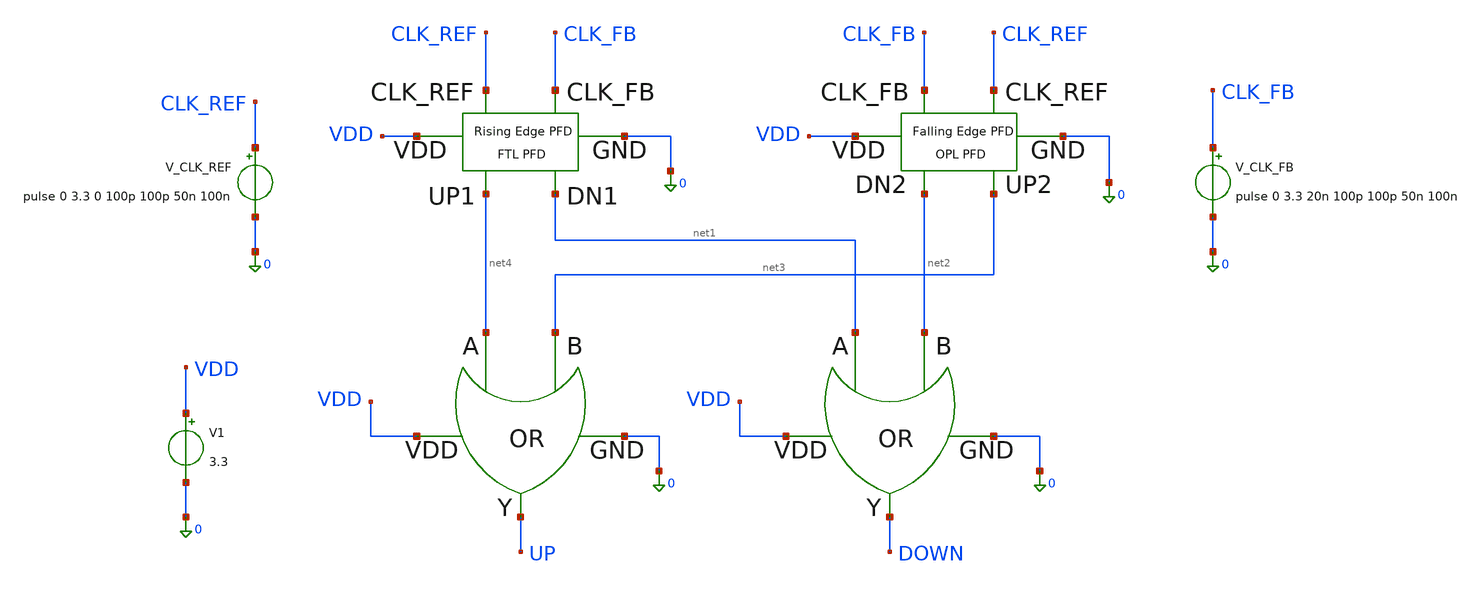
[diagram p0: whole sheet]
** sch_path: PFD/DELD_PFD.sch
**.subckt DELD_PFD
x1 0 net1 net2 VDD DOWN OR
x2 0 net4 net3 VDD UP OR
x3 net1 net4 CLK_FB CLK_REF VDD 0 FTL_PFD
x4 net3 net2 CLK_REF CLK_FB VDD 0 OPL_PFD
V1 VDD 0 3.3
.save i(v1)
V_CLK_REF CLK_REF 0 pulse 0 3.3 0 100p 100p 50n 100n
.save i(v_clk_ref)
V_CLK_FB CLK_FB 0 pulse 0 3.3 20n 100p 100p 50n 100n
.save i(v_clk_fb)
**.ends

* expanding   symbol:  OR.sym # of pins=5
** sym_path: PFD/OR.sym
** sch_path: PFD/OR.sch
.subckt OR GND A B VDD Y
*.opin Y
*.ipin GND
*.ipin VDD
*.ipin A
*.ipin B
XM3 net2 A GND GND nfet_03v3 L=0.28u W=0.22u nf=1 ad='int((nf+1)/2) * W/nf * 0.18u' as='int((nf+2)/2) * W/nf * 0.18u'
+ pd='2*int((nf+1)/2) * (W/nf + 0.18u)' ps='2*int((nf+2)/2) * (W/nf + 0.18u)' nrd='0.18u / W' nrs='0.18u / W'
+ sa=0 sb=0 sd=0 m=1
XM2 net1 A VDD VDD pfet_03v3 L=0.28u W=0.22u nf=1 ad='int((nf+1)/2) * W/nf * 0.18u' as='int((nf+2)/2) * W/nf * 0.18u'
+ pd='2*int((nf+1)/2) * (W/nf + 0.18u)' ps='2*int((nf+2)/2) * (W/nf + 0.18u)' nrd='0.18u / W' nrs='0.18u / W'
+ sa=0 sb=0 sd=0 m=3
XM4 net2 B net1 VDD pfet_03v3 L=0.28u W=0.22u nf=1 ad='int((nf+1)/2) * W/nf * 0.18u' as='int((nf+2)/2) * W/nf * 0.18u'
+ pd='2*int((nf+1)/2) * (W/nf + 0.18u)' ps='2*int((nf+2)/2) * (W/nf + 0.18u)' nrd='0.18u / W' nrs='0.18u / W'
+ sa=0 sb=0 sd=0 m=3
XM1 net2 B GND GND nfet_03v3 L=0.28u W=0.22u nf=1 ad='int((nf+1)/2) * W/nf * 0.18u' as='int((nf+2)/2) * W/nf * 0.18u'
+ pd='2*int((nf+1)/2) * (W/nf + 0.18u)' ps='2*int((nf+2)/2) * (W/nf + 0.18u)' nrd='0.18u / W' nrs='0.18u / W'
+ sa=0 sb=0 sd=0 m=1
XM29 Y net2 VDD VDD pfet_03v3 L=0.28u W=0.22u nf=1 ad='int((nf+1)/2) * W/nf * 0.18u' as='int((nf+2)/2) * W/nf * 0.18u'
+ pd='2*int((nf+1)/2) * (W/nf + 0.18u)' ps='2*int((nf+2)/2) * (W/nf + 0.18u)' nrd='0.18u / W' nrs='0.18u / W'
+ sa=0 sb=0 sd=0 m=3
XM30 Y net2 GND GND nfet_03v3 L=0.28u W=0.22u nf=1 ad='int((nf+1)/2) * W/nf * 0.18u' as='int((nf+2)/2) * W/nf * 0.18u'
+ pd='2*int((nf+1)/2) * (W/nf + 0.18u)' ps='2*int((nf+2)/2) * (W/nf + 0.18u)' nrd='0.18u / W' nrs='0.18u / W'
+ sa=0 sb=0 sd=0 m=1
.ends


* expanding   symbol:  FTL_PFD.sym # of pins=6
** sym_path: PFD/FTL_PFD.sym
** sch_path: PFD/FTL_PFD.sch
.subckt FTL_PFD DN1 UP1 CLK_FB CLK_REF VDD GND
*.opin UP1
*.opin DN1
*.ipin CLK_FB
*.ipin CLK_REF
*.iopin VDD
*.iopin GND
XM1 net1 net3 VDD VDD pfet_03v3 L=0.28u W=0.22u nf=1 ad='int((nf+1)/2) * W/nf * 0.18u' as='int((nf+2)/2) * W/nf * 0.18u'
+ pd='2*int((nf+1)/2) * (W/nf + 0.18u)' ps='2*int((nf+2)/2) * (W/nf + 0.18u)' nrd='0.18u / W' nrs='0.18u / W'
+ sa=0 sb=0 sd=0 m=1
XM4 net2 net3 GND GND nfet_03v3 L=0.28u W=0.22u nf=1 ad='int((nf+1)/2) * W/nf * 0.18u' as='int((nf+2)/2) * W/nf * 0.18u'
+ pd='2*int((nf+1)/2) * (W/nf + 0.18u)' ps='2*int((nf+2)/2) * (W/nf + 0.18u)' nrd='0.18u / W' nrs='0.18u / W'
+ sa=0 sb=0 sd=0 m=1
XM2 net2 CLK_REF net1 VDD pfet_03v3 L=0.28u W=0.22u nf=1 ad='int((nf+1)/2) * W/nf * 0.18u' as='int((nf+2)/2) * W/nf * 0.18u'
+ pd='2*int((nf+1)/2) * (W/nf + 0.18u)' ps='2*int((nf+2)/2) * (W/nf + 0.18u)' nrd='0.18u / W' nrs='0.18u / W'
+ sa=0 sb=0 sd=0 m=1
XM3 net2 CLK_REF GND GND nfet_03v3 L=0.28u W=0.22u nf=1 ad='int((nf+1)/2) * W/nf * 0.18u' as='int((nf+2)/2) * W/nf * 0.18u'
+ pd='2*int((nf+1)/2) * (W/nf + 0.18u)' ps='2*int((nf+2)/2) * (W/nf + 0.18u)' nrd='0.18u / W' nrs='0.18u / W'
+ sa=0 sb=0 sd=0 m=1
XM5 net4 net2 VDD VDD pfet_03v3 L=0.28u W=0.22u nf=1 ad='int((nf+1)/2) * W/nf * 0.18u' as='int((nf+2)/2) * W/nf * 0.18u'
+ pd='2*int((nf+1)/2) * (W/nf + 0.18u)' ps='2*int((nf+2)/2) * (W/nf + 0.18u)' nrd='0.18u / W' nrs='0.18u / W'
+ sa=0 sb=0 sd=0 m=1
XM6 net5 CLK_REF net4 VDD pfet_03v3 L=0.28u W=0.22u nf=1 ad='int((nf+1)/2) * W/nf * 0.18u' as='int((nf+2)/2) * W/nf * 0.18u'
+ pd='2*int((nf+1)/2) * (W/nf + 0.18u)' ps='2*int((nf+2)/2) * (W/nf + 0.18u)' nrd='0.18u / W' nrs='0.18u / W'
+ sa=0 sb=0 sd=0 m=1
XM7 net5 net2 GND GND nfet_03v3 L=0.28u W=0.22u nf=1 ad='int((nf+1)/2) * W/nf * 0.18u' as='int((nf+2)/2) * W/nf * 0.18u'
+ pd='2*int((nf+1)/2) * (W/nf + 0.18u)' ps='2*int((nf+2)/2) * (W/nf + 0.18u)' nrd='0.18u / W' nrs='0.18u / W'
+ sa=0 sb=0 sd=0 m=1
XM9 net6 CLK_REF_bar VDD VDD pfet_03v3 L=0.28u W=0.22u nf=1 ad='int((nf+1)/2) * W/nf * 0.18u' as='int((nf+2)/2) * W/nf * 0.18u'
+ pd='2*int((nf+1)/2) * (W/nf + 0.18u)' ps='2*int((nf+2)/2) * (W/nf + 0.18u)' nrd='0.18u / W' nrs='0.18u / W'
+ sa=0 sb=0 sd=0 m=1
XM10 net7 net5 GND GND nfet_03v3 L=0.28u W=0.22u nf=1 ad='int((nf+1)/2) * W/nf * 0.18u' as='int((nf+2)/2) * W/nf * 0.18u'
+ pd='2*int((nf+1)/2) * (W/nf + 0.18u)' ps='2*int((nf+2)/2) * (W/nf + 0.18u)' nrd='0.18u / W' nrs='0.18u / W'
+ sa=0 sb=0 sd=0 m=1
XM8 net7 net5 net6 VDD pfet_03v3 L=0.28u W=0.22u nf=1 ad='int((nf+1)/2) * W/nf * 0.18u' as='int((nf+2)/2) * W/nf * 0.18u'
+ pd='2*int((nf+1)/2) * (W/nf + 0.18u)' ps='2*int((nf+2)/2) * (W/nf + 0.18u)' nrd='0.18u / W' nrs='0.18u / W'
+ sa=0 sb=0 sd=0 m=1
XM11 net7 CLK_REF_bar GND GND nfet_03v3 L=0.28u W=0.22u nf=1 ad='int((nf+1)/2) * W/nf * 0.18u' as='int((nf+2)/2) * W/nf * 0.18u'
+ pd='2*int((nf+1)/2) * (W/nf + 0.18u)' ps='2*int((nf+2)/2) * (W/nf + 0.18u)' nrd='0.18u / W' nrs='0.18u / W'
+ sa=0 sb=0 sd=0 m=1
XM12 net8 net7 VDD VDD pfet_03v3 L=0.28u W=0.22u nf=1 ad='int((nf+1)/2) * W/nf * 0.18u' as='int((nf+2)/2) * W/nf * 0.18u'
+ pd='2*int((nf+1)/2) * (W/nf + 0.18u)' ps='2*int((nf+2)/2) * (W/nf + 0.18u)' nrd='0.18u / W' nrs='0.18u / W'
+ sa=0 sb=0 sd=0 m=1
XM13 UP1 CLK_REF_bar net8 VDD pfet_03v3 L=0.28u W=0.22u nf=1 ad='int((nf+1)/2) * W/nf * 0.18u' as='int((nf+2)/2) * W/nf * 0.18u'
+ pd='2*int((nf+1)/2) * (W/nf + 0.18u)' ps='2*int((nf+2)/2) * (W/nf + 0.18u)' nrd='0.18u / W' nrs='0.18u / W'
+ sa=0 sb=0 sd=0 m=1
XM14 UP1 net7 GND GND nfet_03v3 L=0.28u W=0.22u nf=1 ad='int((nf+1)/2) * W/nf * 0.18u' as='int((nf+2)/2) * W/nf * 0.18u'
+ pd='2*int((nf+1)/2) * (W/nf + 0.18u)' ps='2*int((nf+2)/2) * (W/nf + 0.18u)' nrd='0.18u / W' nrs='0.18u / W'
+ sa=0 sb=0 sd=0 m=1
XM15 net9 net3 VDD VDD pfet_03v3 L=0.28u W=0.22u nf=1 ad='int((nf+1)/2) * W/nf * 0.18u' as='int((nf+2)/2) * W/nf * 0.18u'
+ pd='2*int((nf+1)/2) * (W/nf + 0.18u)' ps='2*int((nf+2)/2) * (W/nf + 0.18u)' nrd='0.18u / W' nrs='0.18u / W'
+ sa=0 sb=0 sd=0 m=1
XM16 net10 net3 GND GND nfet_03v3 L=0.28u W=0.22u nf=1 ad='int((nf+1)/2) * W/nf * 0.18u' as='int((nf+2)/2) * W/nf * 0.18u'
+ pd='2*int((nf+1)/2) * (W/nf + 0.18u)' ps='2*int((nf+2)/2) * (W/nf + 0.18u)' nrd='0.18u / W' nrs='0.18u / W'
+ sa=0 sb=0 sd=0 m=1
XM17 net10 CLK_FB net9 VDD pfet_03v3 L=0.28u W=0.22u nf=1 ad='int((nf+1)/2) * W/nf * 0.18u' as='int((nf+2)/2) * W/nf * 0.18u'
+ pd='2*int((nf+1)/2) * (W/nf + 0.18u)' ps='2*int((nf+2)/2) * (W/nf + 0.18u)' nrd='0.18u / W' nrs='0.18u / W'
+ sa=0 sb=0 sd=0 m=1
XM18 net10 CLK_FB GND GND nfet_03v3 L=0.28u W=0.22u nf=1 ad='int((nf+1)/2) * W/nf * 0.18u' as='int((nf+2)/2) * W/nf * 0.18u'
+ pd='2*int((nf+1)/2) * (W/nf + 0.18u)' ps='2*int((nf+2)/2) * (W/nf + 0.18u)' nrd='0.18u / W' nrs='0.18u / W'
+ sa=0 sb=0 sd=0 m=1
XM19 net11 net10 VDD VDD pfet_03v3 L=0.28u W=0.22u nf=1 ad='int((nf+1)/2) * W/nf * 0.18u' as='int((nf+2)/2) * W/nf * 0.18u'
+ pd='2*int((nf+1)/2) * (W/nf + 0.18u)' ps='2*int((nf+2)/2) * (W/nf + 0.18u)' nrd='0.18u / W' nrs='0.18u / W'
+ sa=0 sb=0 sd=0 m=1
XM20 net12 CLK_FB net11 VDD pfet_03v3 L=0.28u W=0.22u nf=1 ad='int((nf+1)/2) * W/nf * 0.18u' as='int((nf+2)/2) * W/nf * 0.18u'
+ pd='2*int((nf+1)/2) * (W/nf + 0.18u)' ps='2*int((nf+2)/2) * (W/nf + 0.18u)' nrd='0.18u / W' nrs='0.18u / W'
+ sa=0 sb=0 sd=0 m=1
XM21 net12 net10 GND GND nfet_03v3 L=0.28u W=0.22u nf=1 ad='int((nf+1)/2) * W/nf * 0.18u' as='int((nf+2)/2) * W/nf * 0.18u'
+ pd='2*int((nf+1)/2) * (W/nf + 0.18u)' ps='2*int((nf+2)/2) * (W/nf + 0.18u)' nrd='0.18u / W' nrs='0.18u / W'
+ sa=0 sb=0 sd=0 m=1
XM22 net13 CLK_FB_bar VDD VDD pfet_03v3 L=0.28u W=0.22u nf=1 ad='int((nf+1)/2) * W/nf * 0.18u' as='int((nf+2)/2) * W/nf * 0.18u'
+ pd='2*int((nf+1)/2) * (W/nf + 0.18u)' ps='2*int((nf+2)/2) * (W/nf + 0.18u)' nrd='0.18u / W' nrs='0.18u / W'
+ sa=0 sb=0 sd=0 m=1
XM23 net14 net12 GND GND nfet_03v3 L=0.28u W=0.22u nf=1 ad='int((nf+1)/2) * W/nf * 0.18u' as='int((nf+2)/2) * W/nf * 0.18u'
+ pd='2*int((nf+1)/2) * (W/nf + 0.18u)' ps='2*int((nf+2)/2) * (W/nf + 0.18u)' nrd='0.18u / W' nrs='0.18u / W'
+ sa=0 sb=0 sd=0 m=1
XM24 net14 net12 net13 VDD pfet_03v3 L=0.28u W=0.22u nf=1 ad='int((nf+1)/2) * W/nf * 0.18u' as='int((nf+2)/2) * W/nf * 0.18u'
+ pd='2*int((nf+1)/2) * (W/nf + 0.18u)' ps='2*int((nf+2)/2) * (W/nf + 0.18u)' nrd='0.18u / W' nrs='0.18u / W'
+ sa=0 sb=0 sd=0 m=1
XM25 net14 CLK_FB_bar GND GND nfet_03v3 L=0.28u W=0.22u nf=1 ad='int((nf+1)/2) * W/nf * 0.18u' as='int((nf+2)/2) * W/nf * 0.18u'
+ pd='2*int((nf+1)/2) * (W/nf + 0.18u)' ps='2*int((nf+2)/2) * (W/nf + 0.18u)' nrd='0.18u / W' nrs='0.18u / W'
+ sa=0 sb=0 sd=0 m=1
XM26 net15 net14 VDD VDD pfet_03v3 L=0.28u W=0.22u nf=1 ad='int((nf+1)/2) * W/nf * 0.18u' as='int((nf+2)/2) * W/nf * 0.18u'
+ pd='2*int((nf+1)/2) * (W/nf + 0.18u)' ps='2*int((nf+2)/2) * (W/nf + 0.18u)' nrd='0.18u / W' nrs='0.18u / W'
+ sa=0 sb=0 sd=0 m=1
XM27 DN1 CLK_FB_bar net15 VDD pfet_03v3 L=0.28u W=0.22u nf=1 ad='int((nf+1)/2) * W/nf * 0.18u' as='int((nf+2)/2) * W/nf * 0.18u'
+ pd='2*int((nf+1)/2) * (W/nf + 0.18u)' ps='2*int((nf+2)/2) * (W/nf + 0.18u)' nrd='0.18u / W' nrs='0.18u / W'
+ sa=0 sb=0 sd=0 m=1
XM28 DN1 net14 GND GND nfet_03v3 L=0.28u W=0.22u nf=1 ad='int((nf+1)/2) * W/nf * 0.18u' as='int((nf+2)/2) * W/nf * 0.18u'
+ pd='2*int((nf+1)/2) * (W/nf + 0.18u)' ps='2*int((nf+2)/2) * (W/nf + 0.18u)' nrd='0.18u / W' nrs='0.18u / W'
+ sa=0 sb=0 sd=0 m=1
x1 GND UP1 DN1 net16 net3 XNOR
XM29 CLK_FB_bar CLK_FB VDD VDD pfet_03v3 L=0.28u W=0.22u nf=1 ad='int((nf+1)/2) * W/nf * 0.18u' as='int((nf+2)/2) * W/nf * 0.18u'
+ pd='2*int((nf+1)/2) * (W/nf + 0.18u)' ps='2*int((nf+2)/2) * (W/nf + 0.18u)' nrd='0.18u / W' nrs='0.18u / W'
+ sa=0 sb=0 sd=0 m=3
XM30 CLK_FB_bar CLK_FB GND GND nfet_03v3 L=0.28u W=0.22u nf=1 ad='int((nf+1)/2) * W/nf * 0.18u' as='int((nf+2)/2) * W/nf * 0.18u'
+ pd='2*int((nf+1)/2) * (W/nf + 0.18u)' ps='2*int((nf+2)/2) * (W/nf + 0.18u)' nrd='0.18u / W' nrs='0.18u / W'
+ sa=0 sb=0 sd=0 m=1
XM31 CLK_REF_bar CLK_REF VDD VDD pfet_03v3 L=0.28u W=0.22u nf=1 ad='int((nf+1)/2) * W/nf * 0.18u' as='int((nf+2)/2) * W/nf * 0.18u'
+ pd='2*int((nf+1)/2) * (W/nf + 0.18u)' ps='2*int((nf+2)/2) * (W/nf + 0.18u)' nrd='0.18u / W' nrs='0.18u / W'
+ sa=0 sb=0 sd=0 m=3
XM32 CLK_REF_bar CLK_REF GND GND nfet_03v3 L=0.28u W=0.22u nf=1 ad='int((nf+1)/2) * W/nf * 0.18u' as='int((nf+2)/2) * W/nf * 0.18u'
+ pd='2*int((nf+1)/2) * (W/nf + 0.18u)' ps='2*int((nf+2)/2) * (W/nf + 0.18u)' nrd='0.18u / W' nrs='0.18u / W'
+ sa=0 sb=0 sd=0 m=1
.ends


* expanding   symbol:  OPL_PFD.sym # of pins=6
** sym_path: PFD/OPL_PFD.sym
** sch_path: PFD/OPL_PFD.sch
.subckt OPL_PFD UP2 DN2 CLK_REF CLK_FB VDD GND
*.opin UP2
*.ipin CLK_FB
*.ipin CLK_REF
*.opin DN2
*.iopin VDD
*.iopin GND
XM1 net1 net3 VDD VDD pfet_03v3 L=0.28u W=0.22u nf=1 ad='int((nf+1)/2) * W/nf * 0.18u' as='int((nf+2)/2) * W/nf * 0.18u'
+ pd='2*int((nf+1)/2) * (W/nf + 0.18u)' ps='2*int((nf+2)/2) * (W/nf + 0.18u)' nrd='0.18u / W' nrs='0.18u / W'
+ sa=0 sb=0 sd=0 m=1
XM4 net2 net3 GND GND nfet_03v3 L=0.28u W=0.22u nf=1 ad='int((nf+1)/2) * W/nf * 0.18u' as='int((nf+2)/2) * W/nf * 0.18u'
+ pd='2*int((nf+1)/2) * (W/nf + 0.18u)' ps='2*int((nf+2)/2) * (W/nf + 0.18u)' nrd='0.18u / W' nrs='0.18u / W'
+ sa=0 sb=0 sd=0 m=1
XM5 net4 net1 VDD VDD pfet_03v3 L=0.28u W=0.22u nf=1 ad='int((nf+1)/2) * W/nf * 0.18u' as='int((nf+2)/2) * W/nf * 0.18u'
+ pd='2*int((nf+1)/2) * (W/nf + 0.18u)' ps='2*int((nf+2)/2) * (W/nf + 0.18u)' nrd='0.18u / W' nrs='0.18u / W'
+ sa=0 sb=0 sd=0 m=1
XM7 net5 net1 GND GND nfet_03v3 L=0.28u W=0.22u nf=1 ad='int((nf+1)/2) * W/nf * 0.18u' as='int((nf+2)/2) * W/nf * 0.18u'
+ pd='2*int((nf+1)/2) * (W/nf + 0.18u)' ps='2*int((nf+2)/2) * (W/nf + 0.18u)' nrd='0.18u / W' nrs='0.18u / W'
+ sa=0 sb=0 sd=0 m=1
XM9 CLK_REF_bar CLK_REF_bar VDD VDD pfet_03v3 L=0.28u W=0.22u nf=1 ad='int((nf+1)/2) * W/nf * 0.18u'
+ as='int((nf+2)/2) * W/nf * 0.18u' pd='2*int((nf+1)/2) * (W/nf + 0.18u)' ps='2*int((nf+2)/2) * (W/nf + 0.18u)'
+ nrd='0.18u / W' nrs='0.18u / W' sa=0 sb=0 sd=0 m=1
XM11 net12 CLK_REF_bar GND GND nfet_03v3 L=0.28u W=0.22u nf=1 ad='int((nf+1)/2) * W/nf * 0.18u' as='int((nf+2)/2) * W/nf * 0.18u'
+ pd='2*int((nf+1)/2) * (W/nf + 0.18u)' ps='2*int((nf+2)/2) * (W/nf + 0.18u)' nrd='0.18u / W' nrs='0.18u / W'
+ sa=0 sb=0 sd=0 m=1
XM12 net10 CLK_REF_bar VDD VDD pfet_03v3 L=0.28u W=0.22u nf=1 ad='int((nf+1)/2) * W/nf * 0.18u' as='int((nf+2)/2) * W/nf * 0.18u'
+ pd='2*int((nf+1)/2) * (W/nf + 0.18u)' ps='2*int((nf+2)/2) * (W/nf + 0.18u)' nrd='0.18u / W' nrs='0.18u / W'
+ sa=0 sb=0 sd=0 m=1
XM14 net11 CLK_REF_bar GND GND nfet_03v3 L=0.28u W=0.22u nf=1 ad='int((nf+1)/2) * W/nf * 0.18u' as='int((nf+2)/2) * W/nf * 0.18u'
+ pd='2*int((nf+1)/2) * (W/nf + 0.18u)' ps='2*int((nf+2)/2) * (W/nf + 0.18u)' nrd='0.18u / W' nrs='0.18u / W'
+ sa=0 sb=0 sd=0 m=1
XM2 net1 CLK_REF VDD VDD pfet_03v3 L=0.28u W=0.22u nf=1 ad='int((nf+1)/2) * W/nf * 0.18u' as='int((nf+2)/2) * W/nf * 0.18u'
+ pd='2*int((nf+1)/2) * (W/nf + 0.18u)' ps='2*int((nf+2)/2) * (W/nf + 0.18u)' nrd='0.18u / W' nrs='0.18u / W'
+ sa=0 sb=0 sd=0 m=1
XM6 net4 CLK_REF net5 GND nfet_03v3 L=0.28u W=0.22u nf=1 ad='int((nf+1)/2) * W/nf * 0.18u' as='int((nf+2)/2) * W/nf * 0.18u'
+ pd='2*int((nf+1)/2) * (W/nf + 0.18u)' ps='2*int((nf+2)/2) * (W/nf + 0.18u)' nrd='0.18u / W' nrs='0.18u / W'
+ sa=0 sb=0 sd=0 m=1
XM10 CLK_REF_bar net4 net12 GND nfet_03v3 L=0.28u W=0.22u nf=1 ad='int((nf+1)/2) * W/nf * 0.18u' as='int((nf+2)/2) * W/nf * 0.18u'
+ pd='2*int((nf+1)/2) * (W/nf + 0.18u)' ps='2*int((nf+2)/2) * (W/nf + 0.18u)' nrd='0.18u / W' nrs='0.18u / W'
+ sa=0 sb=0 sd=0 m=1
XM8 CLK_REF_bar net4 VDD VDD pfet_03v3 L=0.28u W=0.22u nf=1 ad='int((nf+1)/2) * W/nf * 0.18u' as='int((nf+2)/2) * W/nf * 0.18u'
+ pd='2*int((nf+1)/2) * (W/nf + 0.18u)' ps='2*int((nf+2)/2) * (W/nf + 0.18u)' nrd='0.18u / W' nrs='0.18u / W'
+ sa=0 sb=0 sd=0 m=1
XM13 net10 CLK_REF_bar net11 GND nfet_03v3 L=0.28u W=0.22u nf=1 ad='int((nf+1)/2) * W/nf * 0.18u' as='int((nf+2)/2) * W/nf * 0.18u'
+ pd='2*int((nf+1)/2) * (W/nf + 0.18u)' ps='2*int((nf+2)/2) * (W/nf + 0.18u)' nrd='0.18u / W' nrs='0.18u / W'
+ sa=0 sb=0 sd=0 m=1
XM15 UP2 net11 VDD VDD pfet_03v3 L=0.28u W=0.22u nf=1 ad='int((nf+1)/2) * W/nf * 0.18u' as='int((nf+2)/2) * W/nf * 0.18u'
+ pd='2*int((nf+1)/2) * (W/nf + 0.18u)' ps='2*int((nf+2)/2) * (W/nf + 0.18u)' nrd='0.18u / W' nrs='0.18u / W'
+ sa=0 sb=0 sd=0 m=3
XM16 UP2 net11 GND GND nfet_03v3 L=0.28u W=0.22u nf=1 ad='int((nf+1)/2) * W/nf * 0.18u' as='int((nf+2)/2) * W/nf * 0.18u'
+ pd='2*int((nf+1)/2) * (W/nf + 0.18u)' ps='2*int((nf+2)/2) * (W/nf + 0.18u)' nrd='0.18u / W' nrs='0.18u / W'
+ sa=0 sb=0 sd=0 m=1
XM17 CLK_FB_bar CLK_FB VDD VDD pfet_03v3 L=0.28u W=0.22u nf=1 ad='int((nf+1)/2) * W/nf * 0.18u' as='int((nf+2)/2) * W/nf * 0.18u'
+ pd='2*int((nf+1)/2) * (W/nf + 0.18u)' ps='2*int((nf+2)/2) * (W/nf + 0.18u)' nrd='0.18u / W' nrs='0.18u / W'
+ sa=0 sb=0 sd=0 m=3
XM18 CLK_FB_bar CLK_FB GND GND nfet_03v3 L=0.28u W=0.22u nf=1 ad='int((nf+1)/2) * W/nf * 0.18u' as='int((nf+2)/2) * W/nf * 0.18u'
+ pd='2*int((nf+1)/2) * (W/nf + 0.18u)' ps='2*int((nf+2)/2) * (W/nf + 0.18u)' nrd='0.18u / W' nrs='0.18u / W'
+ sa=0 sb=0 sd=0 m=1
XM19 CLK_REF_bar CLK_REF VDD VDD pfet_03v3 L=0.28u W=0.22u nf=1 ad='int((nf+1)/2) * W/nf * 0.18u' as='int((nf+2)/2) * W/nf * 0.18u'
+ pd='2*int((nf+1)/2) * (W/nf + 0.18u)' ps='2*int((nf+2)/2) * (W/nf + 0.18u)' nrd='0.18u / W' nrs='0.18u / W'
+ sa=0 sb=0 sd=0 m=3
XM20 CLK_REF_bar CLK_REF GND GND nfet_03v3 L=0.28u W=0.22u nf=1 ad='int((nf+1)/2) * W/nf * 0.18u' as='int((nf+2)/2) * W/nf * 0.18u'
+ pd='2*int((nf+1)/2) * (W/nf + 0.18u)' ps='2*int((nf+2)/2) * (W/nf + 0.18u)' nrd='0.18u / W' nrs='0.18u / W'
+ sa=0 sb=0 sd=0 m=1
XM3 net1 CLK_REF net2 GND nfet_03v3 L=0.28u W=0.22u nf=1 ad='int((nf+1)/2) * W/nf * 0.18u' as='int((nf+2)/2) * W/nf * 0.18u'
+ pd='2*int((nf+1)/2) * (W/nf + 0.18u)' ps='2*int((nf+2)/2) * (W/nf + 0.18u)' nrd='0.18u / W' nrs='0.18u / W'
+ sa=0 sb=0 sd=0 m=1
XM21 net13 net3 VDD VDD pfet_03v3 L=0.28u W=0.22u nf=1 ad='int((nf+1)/2) * W/nf * 0.18u' as='int((nf+2)/2) * W/nf * 0.18u'
+ pd='2*int((nf+1)/2) * (W/nf + 0.18u)' ps='2*int((nf+2)/2) * (W/nf + 0.18u)' nrd='0.18u / W' nrs='0.18u / W'
+ sa=0 sb=0 sd=0 m=1
XM22 net14 net3 GND GND nfet_03v3 L=0.28u W=0.22u nf=1 ad='int((nf+1)/2) * W/nf * 0.18u' as='int((nf+2)/2) * W/nf * 0.18u'
+ pd='2*int((nf+1)/2) * (W/nf + 0.18u)' ps='2*int((nf+2)/2) * (W/nf + 0.18u)' nrd='0.18u / W' nrs='0.18u / W'
+ sa=0 sb=0 sd=0 m=1
XM23 net8 net13 VDD VDD pfet_03v3 L=0.28u W=0.22u nf=1 ad='int((nf+1)/2) * W/nf * 0.18u' as='int((nf+2)/2) * W/nf * 0.18u'
+ pd='2*int((nf+1)/2) * (W/nf + 0.18u)' ps='2*int((nf+2)/2) * (W/nf + 0.18u)' nrd='0.18u / W' nrs='0.18u / W'
+ sa=0 sb=0 sd=0 m=1
XM24 net15 net13 GND GND nfet_03v3 L=0.28u W=0.22u nf=1 ad='int((nf+1)/2) * W/nf * 0.18u' as='int((nf+2)/2) * W/nf * 0.18u'
+ pd='2*int((nf+1)/2) * (W/nf + 0.18u)' ps='2*int((nf+2)/2) * (W/nf + 0.18u)' nrd='0.18u / W' nrs='0.18u / W'
+ sa=0 sb=0 sd=0 m=1
XM25 net9 CLK_FB_bar VDD VDD pfet_03v3 L=0.28u W=0.22u nf=1 ad='int((nf+1)/2) * W/nf * 0.18u' as='int((nf+2)/2) * W/nf * 0.18u'
+ pd='2*int((nf+1)/2) * (W/nf + 0.18u)' ps='2*int((nf+2)/2) * (W/nf + 0.18u)' nrd='0.18u / W' nrs='0.18u / W'
+ sa=0 sb=0 sd=0 m=1
XM26 net6 CLK_FB_bar GND GND nfet_03v3 L=0.28u W=0.22u nf=1 ad='int((nf+1)/2) * W/nf * 0.18u' as='int((nf+2)/2) * W/nf * 0.18u'
+ pd='2*int((nf+1)/2) * (W/nf + 0.18u)' ps='2*int((nf+2)/2) * (W/nf + 0.18u)' nrd='0.18u / W' nrs='0.18u / W'
+ sa=0 sb=0 sd=0 m=1
XM27 net16 net9 VDD VDD pfet_03v3 L=0.28u W=0.22u nf=1 ad='int((nf+1)/2) * W/nf * 0.18u' as='int((nf+2)/2) * W/nf * 0.18u'
+ pd='2*int((nf+1)/2) * (W/nf + 0.18u)' ps='2*int((nf+2)/2) * (W/nf + 0.18u)' nrd='0.18u / W' nrs='0.18u / W'
+ sa=0 sb=0 sd=0 m=1
XM28 net7 net9 GND GND nfet_03v3 L=0.28u W=0.22u nf=1 ad='int((nf+1)/2) * W/nf * 0.18u' as='int((nf+2)/2) * W/nf * 0.18u'
+ pd='2*int((nf+1)/2) * (W/nf + 0.18u)' ps='2*int((nf+2)/2) * (W/nf + 0.18u)' nrd='0.18u / W' nrs='0.18u / W'
+ sa=0 sb=0 sd=0 m=1
XM29 net13 CLK_FB VDD VDD pfet_03v3 L=0.28u W=0.22u nf=1 ad='int((nf+1)/2) * W/nf * 0.18u' as='int((nf+2)/2) * W/nf * 0.18u'
+ pd='2*int((nf+1)/2) * (W/nf + 0.18u)' ps='2*int((nf+2)/2) * (W/nf + 0.18u)' nrd='0.18u / W' nrs='0.18u / W'
+ sa=0 sb=0 sd=0 m=1
XM30 net8 CLK_FB net15 GND nfet_03v3 L=0.28u W=0.22u nf=1 ad='int((nf+1)/2) * W/nf * 0.18u' as='int((nf+2)/2) * W/nf * 0.18u'
+ pd='2*int((nf+1)/2) * (W/nf + 0.18u)' ps='2*int((nf+2)/2) * (W/nf + 0.18u)' nrd='0.18u / W' nrs='0.18u / W'
+ sa=0 sb=0 sd=0 m=1
XM31 net9 net8 net6 GND nfet_03v3 L=0.28u W=0.22u nf=1 ad='int((nf+1)/2) * W/nf * 0.18u' as='int((nf+2)/2) * W/nf * 0.18u'
+ pd='2*int((nf+1)/2) * (W/nf + 0.18u)' ps='2*int((nf+2)/2) * (W/nf + 0.18u)' nrd='0.18u / W' nrs='0.18u / W'
+ sa=0 sb=0 sd=0 m=1
XM32 net9 net8 VDD VDD pfet_03v3 L=0.28u W=0.22u nf=1 ad='int((nf+1)/2) * W/nf * 0.18u' as='int((nf+2)/2) * W/nf * 0.18u'
+ pd='2*int((nf+1)/2) * (W/nf + 0.18u)' ps='2*int((nf+2)/2) * (W/nf + 0.18u)' nrd='0.18u / W' nrs='0.18u / W'
+ sa=0 sb=0 sd=0 m=1
XM33 net16 CLK_FB_bar net7 GND nfet_03v3 L=0.28u W=0.22u nf=1 ad='int((nf+1)/2) * W/nf * 0.18u' as='int((nf+2)/2) * W/nf * 0.18u'
+ pd='2*int((nf+1)/2) * (W/nf + 0.18u)' ps='2*int((nf+2)/2) * (W/nf + 0.18u)' nrd='0.18u / W' nrs='0.18u / W'
+ sa=0 sb=0 sd=0 m=1
XM34 DN2 net7 VDD VDD pfet_03v3 L=0.28u W=0.22u nf=1 ad='int((nf+1)/2) * W/nf * 0.18u' as='int((nf+2)/2) * W/nf * 0.18u'
+ pd='2*int((nf+1)/2) * (W/nf + 0.18u)' ps='2*int((nf+2)/2) * (W/nf + 0.18u)' nrd='0.18u / W' nrs='0.18u / W'
+ sa=0 sb=0 sd=0 m=3
XM35 DN2 net7 GND GND nfet_03v3 L=0.28u W=0.22u nf=1 ad='int((nf+1)/2) * W/nf * 0.18u' as='int((nf+2)/2) * W/nf * 0.18u'
+ pd='2*int((nf+1)/2) * (W/nf + 0.18u)' ps='2*int((nf+2)/2) * (W/nf + 0.18u)' nrd='0.18u / W' nrs='0.18u / W'
+ sa=0 sb=0 sd=0 m=1
XM36 net13 CLK_FB net14 GND nfet_03v3 L=0.28u W=0.22u nf=1 ad='int((nf+1)/2) * W/nf * 0.18u' as='int((nf+2)/2) * W/nf * 0.18u'
+ pd='2*int((nf+1)/2) * (W/nf + 0.18u)' ps='2*int((nf+2)/2) * (W/nf + 0.18u)' nrd='0.18u / W' nrs='0.18u / W'
+ sa=0 sb=0 sd=0 m=1
x1 GND UP2 DN2 VDD net3 NAND
.ends


* expanding   symbol:  XNOR.sym # of pins=5
** sym_path: PFD/XNOR.sym
** sch_path: PFD/XNOR.sch
.subckt XNOR GND A B VDD Y
*.opin Y
*.ipin A
*.ipin B
*.iopin VDD
*.iopin GND
XM1 net1 A VDD VDD pfet_03v3 L=0.28u W=0.22u nf=1 ad='int((nf+1)/2) * W/nf * 0.18u' as='int((nf+2)/2) * W/nf * 0.18u'
+ pd='2*int((nf+1)/2) * (W/nf + 0.18u)' ps='2*int((nf+2)/2) * (W/nf + 0.18u)' nrd='0.18u / W' nrs='0.18u / W'
+ sa=0 sb=0 sd=0 m=1
XM2 Y A_bar net1 VDD pfet_03v3 L=0.28u W=0.22u nf=1 ad='int((nf+1)/2) * W/nf * 0.18u' as='int((nf+2)/2) * W/nf * 0.18u'
+ pd='2*int((nf+1)/2) * (W/nf + 0.18u)' ps='2*int((nf+2)/2) * (W/nf + 0.18u)' nrd='0.18u / W' nrs='0.18u / W'
+ sa=0 sb=0 sd=0 m=1
XM3 Y B_bar net2 GND nfet_03v3 L=0.28u W=0.22u nf=1 ad='int((nf+1)/2) * W/nf * 0.18u' as='int((nf+2)/2) * W/nf * 0.18u'
+ pd='2*int((nf+1)/2) * (W/nf + 0.18u)' ps='2*int((nf+2)/2) * (W/nf + 0.18u)' nrd='0.18u / W' nrs='0.18u / W'
+ sa=0 sb=0 sd=0 m=1
XM4 net2 A GND GND nfet_03v3 L=0.28u W=0.22u nf=1 ad='int((nf+1)/2) * W/nf * 0.18u' as='int((nf+2)/2) * W/nf * 0.18u'
+ pd='2*int((nf+1)/2) * (W/nf + 0.18u)' ps='2*int((nf+2)/2) * (W/nf + 0.18u)' nrd='0.18u / W' nrs='0.18u / W'
+ sa=0 sb=0 sd=0 m=1
XM5 net3 B_bar VDD VDD pfet_03v3 L=0.28u W=0.22u nf=1 ad='int((nf+1)/2) * W/nf * 0.18u' as='int((nf+2)/2) * W/nf * 0.18u'
+ pd='2*int((nf+1)/2) * (W/nf + 0.18u)' ps='2*int((nf+2)/2) * (W/nf + 0.18u)' nrd='0.18u / W' nrs='0.18u / W'
+ sa=0 sb=0 sd=0 m=1
XM6 Y B net3 VDD pfet_03v3 L=0.28u W=0.22u nf=1 ad='int((nf+1)/2) * W/nf * 0.18u' as='int((nf+2)/2) * W/nf * 0.18u'
+ pd='2*int((nf+1)/2) * (W/nf + 0.18u)' ps='2*int((nf+2)/2) * (W/nf + 0.18u)' nrd='0.18u / W' nrs='0.18u / W'
+ sa=0 sb=0 sd=0 m=1
XM7 Y A_bar net4 GND nfet_03v3 L=0.28u W=0.22u nf=1 ad='int((nf+1)/2) * W/nf * 0.18u' as='int((nf+2)/2) * W/nf * 0.18u'
+ pd='2*int((nf+1)/2) * (W/nf + 0.18u)' ps='2*int((nf+2)/2) * (W/nf + 0.18u)' nrd='0.18u / W' nrs='0.18u / W'
+ sa=0 sb=0 sd=0 m=1
XM8 net4 B GND GND nfet_03v3 L=0.28u W=0.22u nf=1 ad='int((nf+1)/2) * W/nf * 0.18u' as='int((nf+2)/2) * W/nf * 0.18u'
+ pd='2*int((nf+1)/2) * (W/nf + 0.18u)' ps='2*int((nf+2)/2) * (W/nf + 0.18u)' nrd='0.18u / W' nrs='0.18u / W'
+ sa=0 sb=0 sd=0 m=1
XM9 A_bar A VDD VDD pfet_03v3 L=0.28u W=0.22u nf=1 ad='int((nf+1)/2) * W/nf * 0.18u' as='int((nf+2)/2) * W/nf * 0.18u'
+ pd='2*int((nf+1)/2) * (W/nf + 0.18u)' ps='2*int((nf+2)/2) * (W/nf + 0.18u)' nrd='0.18u / W' nrs='0.18u / W'
+ sa=0 sb=0 sd=0 m=3
XM10 A_bar A GND GND nfet_03v3 L=0.28u W=0.22u nf=1 ad='int((nf+1)/2) * W/nf * 0.18u' as='int((nf+2)/2) * W/nf * 0.18u'
+ pd='2*int((nf+1)/2) * (W/nf + 0.18u)' ps='2*int((nf+2)/2) * (W/nf + 0.18u)' nrd='0.18u / W' nrs='0.18u / W'
+ sa=0 sb=0 sd=0 m=1
XM11 B_bar B VDD VDD pfet_03v3 L=0.28u W=0.22u nf=1 ad='int((nf+1)/2) * W/nf * 0.18u' as='int((nf+2)/2) * W/nf * 0.18u'
+ pd='2*int((nf+1)/2) * (W/nf + 0.18u)' ps='2*int((nf+2)/2) * (W/nf + 0.18u)' nrd='0.18u / W' nrs='0.18u / W'
+ sa=0 sb=0 sd=0 m=3
XM12 B_bar B GND GND nfet_03v3 L=0.28u W=0.22u nf=1 ad='int((nf+1)/2) * W/nf * 0.18u' as='int((nf+2)/2) * W/nf * 0.18u'
+ pd='2*int((nf+1)/2) * (W/nf + 0.18u)' ps='2*int((nf+2)/2) * (W/nf + 0.18u)' nrd='0.18u / W' nrs='0.18u / W'
+ sa=0 sb=0 sd=0 m=1
.ends


* expanding   symbol:  NAND.sym # of pins=5
** sym_path: PFD/NAND.sym
** sch_path: PFD/NAND.sch
.subckt NAND GND A B VDD Y
*.opin Y
*.ipin A
*.ipin B
*.iopin VDD
*.iopin GND
XM1 Y A net2 VDD pfet_03v3 L=0.28u W=0.22u nf=1 ad='int((nf+1)/2) * W/nf * 0.18u' as='int((nf+2)/2) * W/nf * 0.18u'
+ pd='2*int((nf+1)/2) * (W/nf + 0.18u)' ps='2*int((nf+2)/2) * (W/nf + 0.18u)' nrd='0.18u / W' nrs='0.18u / W'
+ sa=0 sb=0 sd=0 m=3
XM3 Y A net1 GND nfet_03v3 L=0.28u W=0.22u nf=1 ad='int((nf+1)/2) * W/nf * 0.18u' as='int((nf+2)/2) * W/nf * 0.18u'
+ pd='2*int((nf+1)/2) * (W/nf + 0.18u)' ps='2*int((nf+2)/2) * (W/nf + 0.18u)' nrd='0.18u / W' nrs='0.18u / W'
+ sa=0 sb=0 sd=0 m=1
XM4 net1 B GND GND nfet_03v3 L=0.28u W=0.22u nf=1 ad='int((nf+1)/2) * W/nf * 0.18u' as='int((nf+2)/2) * W/nf * 0.18u'
+ pd='2*int((nf+1)/2) * (W/nf + 0.18u)' ps='2*int((nf+2)/2) * (W/nf + 0.18u)' nrd='0.18u / W' nrs='0.18u / W'
+ sa=0 sb=0 sd=0 m=1
XM2 Y B net3 VDD pfet_03v3 L=0.28u W=0.22u nf=1 ad='int((nf+1)/2) * W/nf * 0.18u' as='int((nf+2)/2) * W/nf * 0.18u'
+ pd='2*int((nf+1)/2) * (W/nf + 0.18u)' ps='2*int((nf+2)/2) * (W/nf + 0.18u)' nrd='0.18u / W' nrs='0.18u / W'
+ sa=0 sb=0 sd=0 m=3
.ends

.end
